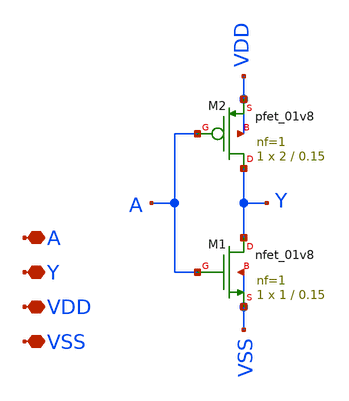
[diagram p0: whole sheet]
** sch_path: takim_adi_FINAL/xschem/inv.sch
**.subckt inv A Y VDD VSS
*.iopin A
*.iopin Y
*.iopin VDD
*.iopin VSS
XM1 Y A VSS VSS sky130_fd_pr__nfet_01v8 L=0.15 W=1 nf=1 ad='int((nf+1)/2) * W/nf * 0.29' as='int((nf+2)/2) * W/nf * 0.29'
+ pd='2*int((nf+1)/2) * (W/nf + 0.29)' ps='2*int((nf+2)/2) * (W/nf + 0.29)' nrd='0.29 / W' nrs='0.29 / W'
+ sa=0 sb=0 sd=0 mult=1 m=1
XM2 Y A VDD VDD sky130_fd_pr__pfet_01v8 L=0.15 W=2 nf=1 ad='int((nf+1)/2) * W/nf * 0.29' as='int((nf+2)/2) * W/nf * 0.29'
+ pd='2*int((nf+1)/2) * (W/nf + 0.29)' ps='2*int((nf+2)/2) * (W/nf + 0.29)' nrd='0.29 / W' nrs='0.29 / W'
+ sa=0 sb=0 sd=0 mult=1 m=1
**.ends
.end
